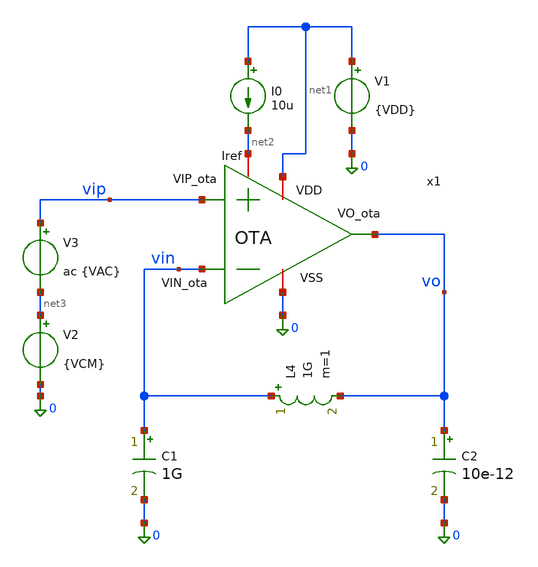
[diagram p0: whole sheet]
** sch_path: xschem/OTA_tb.sch
**.subckt OTA_tb
x1 net1 vo vin vip net2 0 OTA
V1 net1 0 {VDD}
I0 net1 net2 10u
V2 net3 0 {VCM}
V3 vip net3 ac {VAC}
C1 vin 0 1G m=1
L4 vin vo 1G m=1
C2 vo 0 10e-12 m=1
**** begin user architecture code




* 1. Inclusión de libreria de modelos Sky130 PRIMERO
.lib /foss/pdks/sky130A/libs.tech/ngspice/sky130.lib.spice tt

**parametros_ota
.param VDD = 1.8
.param VCM = 1.2
.param VAC = 1



.control

save all
* PMOS
save @m.x1.xMnr.msky130_fd_pr__pfet_01v8[gm]
save @m.x1.xMnr.msky130_fd_pr__pfet_01v8[gds]
save @m.x1.xMnr.msky130_fd_pr__pfet_01v8[id]
save @m.x1.xMnr.msky130_fd_pr__pfet_01v8[vgs]
save @m.x1.xMnr.msky130_fd_pr__pfet_01v8[vds]
save @m.x1.xMnr.msky130_fd_pr__pfet_01v8[vth]
save @m.x1.xMnr.msky130_fd_pr__pfet_01v8[vdsat]

save @m.x1.xMpr.msky130_fd_pr__pfet_01v8[gm]
save @m.x1.xMpr.msky130_fd_pr__pfet_01v8[gds]
save @m.x1.xMpr.msky130_fd_pr__pfet_01v8[id]
save @m.x1.xMpr.msky130_fd_pr__pfet_01v8[vgs]
save @m.x1.xMpr.msky130_fd_pr__pfet_01v8[vds]
save @m.x1.xMpr.msky130_fd_pr__pfet_01v8[vth]
save @m.x1.xMpr.msky130_fd_pr__pfet_01v8[vdsat]

save @m.x1.xMo.msky130_fd_pr__pfet_01v8[gm]
save @m.x1.xMo.msky130_fd_pr__pfet_01v8[gds]
save @m.x1.xMo.msky130_fd_pr__pfet_01v8[id]
save @m.x1.xMo.msky130_fd_pr__pfet_01v8[vgs]
save @m.x1.xMo.msky130_fd_pr__pfet_01v8[vds]
save @m.x1.xMo.msky130_fd_pr__pfet_01v8[vth]
save @m.x1.xMo.msky130_fd_pr__pfet_01v8[vdsat]

* NMOS
save @m.x1.xMn.msky130_fd_pr__nfet_01v8[gm]
save @m.x1.xMn.msky130_fd_pr__nfet_01v8[gds]
save @m.x1.xMn.msky130_fd_pr__nfet_01v8[id]
save @m.x1.xMn.msky130_fd_pr__nfet_01v8[vgs]
save @m.x1.xMn.msky130_fd_pr__nfet_01v8[vds]
save @m.x1.xMn.msky130_fd_pr__nfet_01v8[vth]
save @m.x1.xMn.msky130_fd_pr__nfet_01v8[vdsat]

save @m.x1.xMp.msky130_fd_pr__nfet_01v8[gm]
save @m.x1.xMp.msky130_fd_pr__nfet_01v8[gds]
save @m.x1.xMp.msky130_fd_pr__nfet_01v8[id]
save @m.x1.xMp.msky130_fd_pr__nfet_01v8[vgs]
save @m.x1.xMp.msky130_fd_pr__nfet_01v8[vds]
save @m.x1.xMp.msky130_fd_pr__nfet_01v8[vth]
save @m.x1.xMp.msky130_fd_pr__nfet_01v8[vdsat]

save @m.x1.xMr.msky130_fd_pr__nfet_01v8[gm]
save @m.x1.xMr.msky130_fd_pr__nfet_01v8[gds]
save @m.x1.xMr.msky130_fd_pr__nfet_01v8[id]
save @m.x1.xMr.msky130_fd_pr__nfet_01v8[vgs]
save @m.x1.xMr.msky130_fd_pr__nfet_01v8[vds]
save @m.x1.xMr.msky130_fd_pr__nfet_01v8[vth]
save @m.x1.xMr.msky130_fd_pr__nfet_01v8[vdsat]

save @m.x1.xMrc1.msky130_fd_pr__nfet_01v8[gm]
save @m.x1.xMrc1.msky130_fd_pr__nfet_01v8[gds]
save @m.x1.xMrc1.msky130_fd_pr__nfet_01v8[id]
save @m.x1.xMrc1.msky130_fd_pr__nfet_01v8[vgs]
save @m.x1.xMrc1.msky130_fd_pr__nfet_01v8[vds]
save @m.x1.xMrc1.msky130_fd_pr__nfet_01v8[vth]
save @m.x1.xMrc1.msky130_fd_pr__nfet_01v8[vdsat]

save @m.x1.xMc2.msky130_fd_pr__nfet_01v8[gm]
save @m.x1.xMc2.msky130_fd_pr__nfet_01v8[gds]
save @m.x1.xMc2.msky130_fd_pr__nfet_01v8[id]
save @m.x1.xMc2.msky130_fd_pr__nfet_01v8[vgs]
save @m.x1.xMc2.msky130_fd_pr__nfet_01v8[vds]
save @m.x1.xMc2.msky130_fd_pr__nfet_01v8[vth]
save @m.x1.xMc2.msky130_fd_pr__nfet_01v8[vdsat]

set filetype=ascii
op
write OTA_op.raw

ac dec 10 1 1G
write OTA_ac.raw


* 1. Frecuencia de Corte a -3dB
meas ac f3db WHEN vdb(vo) = vdb(vo)[0] - 3

* 2. UGB (Frecuencia donde la magnitud cruza 0 dB)
meas ac ugb WHEN vdb(vo) = 0

* 3. Crear el vector de fase y convertirlo a grados (multiplicando por 180/pi)
let fase_deg = cph(v(vo)) * 180 / pi

* 4. Medir la fase en grados en el punto exacto del UGB
meas ac fase_ugb FIND fase_deg WHEN vdb(vo) = 0

* 5. Calcular el Margen de Fase automáticamente
let margen_fase = 180 + fase_ugb
print margen_fase

* 6. Graficar la magnitud y la fase ya convertida a grados
plot vdb(vo)
plot fase_deg
.endc


**** end user architecture code
**.ends

* expanding   symbol:  /foss/designs/LDO-sky130/xschem/OTA.sym # of pins=6
** sym_path: xschem/OTA.sym
** sch_path: xschem/OTA.sch
.subckt OTA VDD VO_ota VIN_ota VIP_ota Iref VSS
*.ipin VIN_ota
*.opin VO_ota
*.iopin Iref
*.iopin VSS
*.iopin VDD
*.ipin VIP_ota
XMr Iref Iref VSS VSS sky130_fd_pr__nfet_01v8 L=0.5 W=0.5 nf=1 ad='int((1 + 1)/2) * 0.5 / 1 * 0.29' as='int((1 + 2)/2) * 0.5 / 1 * 0.29'
+ pd='2*int((1 + 1)/2) * (0.5 / 1 + 0.29)' ps='2*int((1 + 2)/2) * (0.5 / 1 + 0.29)' nrd='0.29 / 0.5 ' nrs='0.29 / 0.5 '
+ sa=0 sb=0 sd=0 mult=1 m=1
XMo VO_ota VO_ota1 VDD VDD sky130_fd_pr__pfet_01v8 L=0.5 W=20 nf=1 ad='int((1 + 1)/2) * 20 / 1 * 0.29'
+ as='int((1 + 2)/2) * 20 / 1 * 0.29' pd='2*int((1 + 1)/2) * (20 / 1 + 0.29)' ps='2*int((1 + 2)/2) * (20 / 1 + 0.29)'
+ nrd='0.29 / 20 ' nrs='0.29 / 20 ' sa=0 sb=0 sd=0 mult=1 m=1
XMrc1 Vtail Iref VSS VSS sky130_fd_pr__nfet_01v8 L=0.5 W=2 nf=1 ad='int((1 + 1)/2) * 2 / 1 * 0.29' as='int((1 + 2)/2) * 2 / 1 * 0.29'
+ pd='2*int((1 + 1)/2) * (2 / 1 + 0.29)' ps='2*int((1 + 2)/2) * (2 / 1 + 0.29)' nrd='0.29 / 2 ' nrs='0.29 / 2 '
+ sa=0 sb=0 sd=0 mult=1 m=1
XMc2 VO_ota Iref VSS VSS sky130_fd_pr__nfet_01v8 L=0.5 W=1 nf=1 ad='int((1 + 1)/2) * 1 / 1 * 0.29' as='int((1 + 2)/2) * 1 / 1 * 0.29'
+ pd='2*int((1 + 1)/2) * (1 / 1 + 0.29)' ps='2*int((1 + 2)/2) * (1 / 1 + 0.29)' nrd='0.29 / 1 ' nrs='0.29 / 1 '
+ sa=0 sb=0 sd=0 mult=1 m=1
XMn VGP VIN_ota Vtail VSS sky130_fd_pr__nfet_01v8 L=0.5 W=40 nf=1 ad='int((1 + 1)/2) * 40 / 1 * 0.29'
+ as='int((1 + 2)/2) * 40 / 1 * 0.29' pd='2*int((1 + 1)/2) * (40 / 1 + 0.29)' ps='2*int((1 + 2)/2) * (40 / 1 + 0.29)'
+ nrd='0.29 / 40 ' nrs='0.29 / 40 ' sa=0 sb=0 sd=0 mult=1 m=1
XMp VO_ota1 VIP_ota Vtail VSS sky130_fd_pr__nfet_01v8 L=0.5 W=40 nf=1 ad='int((1 + 1)/2) * 40 / 1 * 0.29'
+ as='int((1 + 2)/2) * 40 / 1 * 0.29' pd='2*int((1 + 1)/2) * (40 / 1 + 0.29)' ps='2*int((1 + 2)/2) * (40 / 1 + 0.29)'
+ nrd='0.29 / 40 ' nrs='0.29 / 40 ' sa=0 sb=0 sd=0 mult=1 m=1
XMpr VO_ota1 VGP VDD VDD sky130_fd_pr__pfet_01v8 L=0.5 W=40 nf=1 ad='int((1 + 1)/2) * 40 / 1 * 0.29'
+ as='int((1 + 2)/2) * 40 / 1 * 0.29' pd='2*int((1 + 1)/2) * (40 / 1 + 0.29)' ps='2*int((1 + 2)/2) * (40 / 1 + 0.29)'
+ nrd='0.29 / 40 ' nrs='0.29 / 40 ' sa=0 sb=0 sd=0 mult=1 m=1
XMnr VGP VGP VDD VDD sky130_fd_pr__pfet_01v8 L=0.5 W=40 nf=1 ad='int((1 + 1)/2) * 40 / 1 * 0.29' as='int((1 + 2)/2) * 40 / 1 * 0.29'
+ pd='2*int((1 + 1)/2) * (40 / 1 + 0.29)' ps='2*int((1 + 2)/2) * (40 / 1 + 0.29)' nrd='0.29 / 40 ' nrs='0.29 / 40 '
+ sa=0 sb=0 sd=0 mult=1 m=1
XR1 VO_ota1 net1 VDD sky130_fd_pr__res_high_po W=0.35 L=360 mult=1 m=1
XC1 VO_ota net1 sky130_fd_pr__cap_mim_m3_2 W=50 L=50 MF=1 m=1
.ends

.end
